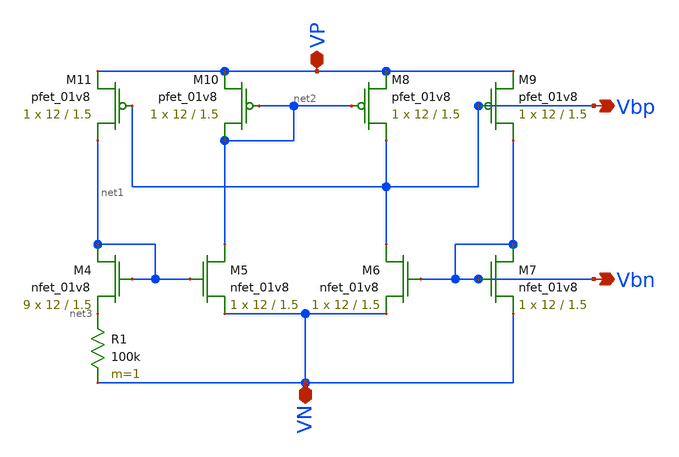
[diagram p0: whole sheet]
** sch_path: mp4_submission/bias_gen/schematics/current_bias.sch
**.subckt current_bias VP VN Vbn Vbp
*.iopin VP
*.iopin VN
*.opin Vbn
*.opin Vbp
XM4 net1 net1 net3 GND sky130_fd_pr__nfet_01v8 L=1.5 W=12 nf=1 ad='int((nf+1)/2) * W/nf * 0.29' as='int((nf+2)/2) * W/nf * 0.29'
+ pd='2*int((nf+1)/2) * (W/nf + 0.29)' ps='2*int((nf+2)/2) * (W/nf + 0.29)' nrd='0.29 / W' nrs='0.29 / W'
+ sa=0 sb=0 sd=0 mult=9 m=9
XM5 net2 net1 VN GND sky130_fd_pr__nfet_01v8 L=1.5 W=12 nf=1 ad='int((nf+1)/2) * W/nf * 0.29' as='int((nf+2)/2) * W/nf * 0.29'
+ pd='2*int((nf+1)/2) * (W/nf + 0.29)' ps='2*int((nf+2)/2) * (W/nf + 0.29)' nrd='0.29 / W' nrs='0.29 / W'
+ sa=0 sb=0 sd=0 mult=1 m=1
XM6 Vbp Vbn VN GND sky130_fd_pr__nfet_01v8 L=1.5 W=12 nf=1 ad='int((nf+1)/2) * W/nf * 0.29' as='int((nf+2)/2) * W/nf * 0.29'
+ pd='2*int((nf+1)/2) * (W/nf + 0.29)' ps='2*int((nf+2)/2) * (W/nf + 0.29)' nrd='0.29 / W' nrs='0.29 / W'
+ sa=0 sb=0 sd=0 mult=1 m=1
XM7 Vbn Vbn VN GND sky130_fd_pr__nfet_01v8 L=1.5 W=12 nf=1 ad='int((nf+1)/2) * W/nf * 0.29' as='int((nf+2)/2) * W/nf * 0.29'
+ pd='2*int((nf+1)/2) * (W/nf + 0.29)' ps='2*int((nf+2)/2) * (W/nf + 0.29)' nrd='0.29 / W' nrs='0.29 / W'
+ sa=0 sb=0 sd=0 mult=1 m=1
R1 net3 VN 100k m=1
XM8 Vbp net2 VP VDD sky130_fd_pr__pfet_01v8 L=1.5 W=12 nf=1 ad='int((nf+1)/2) * W/nf * 0.29' as='int((nf+2)/2) * W/nf * 0.29'
+ pd='2*int((nf+1)/2) * (W/nf + 0.29)' ps='2*int((nf+2)/2) * (W/nf + 0.29)' nrd='0.29 / W' nrs='0.29 / W'
+ sa=0 sb=0 sd=0 mult=1 m=1
XM9 Vbn Vbp VP VDD sky130_fd_pr__pfet_01v8 L=1.5 W=12 nf=1 ad='int((nf+1)/2) * W/nf * 0.29' as='int((nf+2)/2) * W/nf * 0.29'
+ pd='2*int((nf+1)/2) * (W/nf + 0.29)' ps='2*int((nf+2)/2) * (W/nf + 0.29)' nrd='0.29 / W' nrs='0.29 / W'
+ sa=0 sb=0 sd=0 mult=1 m=1
XM10 net2 net2 VP VDD sky130_fd_pr__pfet_01v8 L=1.5 W=12 nf=1 ad='int((nf+1)/2) * W/nf * 0.29' as='int((nf+2)/2) * W/nf * 0.29'
+ pd='2*int((nf+1)/2) * (W/nf + 0.29)' ps='2*int((nf+2)/2) * (W/nf + 0.29)' nrd='0.29 / W' nrs='0.29 / W'
+ sa=0 sb=0 sd=0 mult=1 m=1
XM11 net1 Vbp VP VDD sky130_fd_pr__pfet_01v8 L=1.5 W=12 nf=1 ad='int((nf+1)/2) * W/nf * 0.29' as='int((nf+2)/2) * W/nf * 0.29'
+ pd='2*int((nf+1)/2) * (W/nf + 0.29)' ps='2*int((nf+2)/2) * (W/nf + 0.29)' nrd='0.29 / W' nrs='0.29 / W'
+ sa=0 sb=0 sd=0 mult=1 m=1
**.ends
.end
